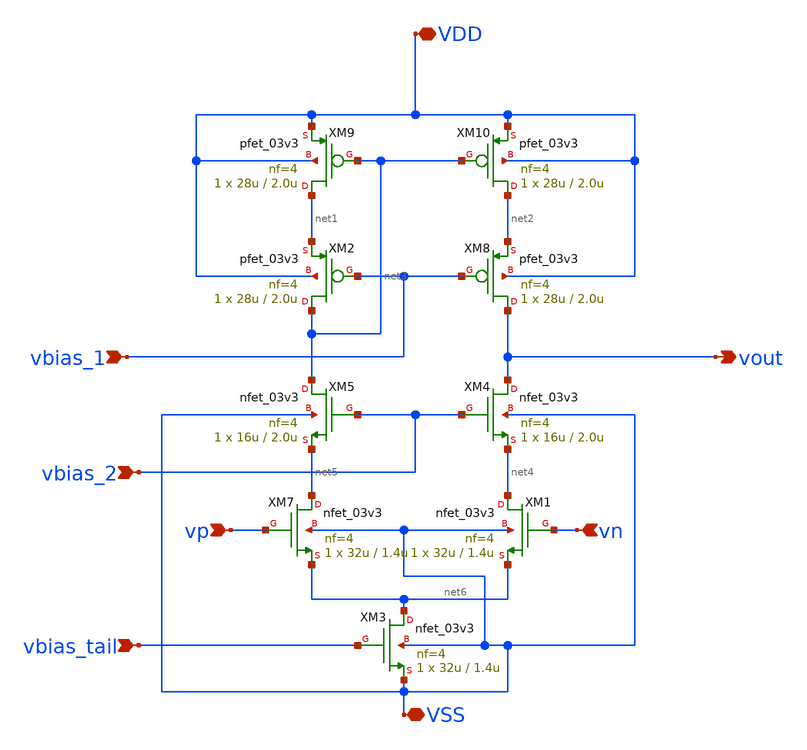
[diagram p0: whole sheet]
** sch_path: xschem/amp_stg_1.sch
**.subckt amp_stg_1 VDD VSS vn vp vout vbias_tail vbias_2 vbias_1
*.iopin VDD
*.iopin VSS
*.ipin vn
*.ipin vp
*.opin vout
*.ipin vbias_tail
*.ipin vbias_2
*.ipin vbias_1
XM2 net3 vbias_1 net1 VDD pfet_03v3 L=2.0u W=28u nf=4 ad='int((nf+1)/2) * W/nf * 0.18u' as='int((nf+2)/2) * W/nf * 0.18u'
+ pd='2*int((nf+1)/2) * (W/nf + 0.18u)' ps='2*int((nf+2)/2) * (W/nf + 0.18u)' nrd='0.18u / W' nrs='0.18u / W'
+ sa=0 sb=0 sd=0 m=1 par=1
XM1 net4 vn net6 VSS nfet_03v3 L=1.4u W=32u nf=4 ad='int((nf+1)/2) * W/nf * 0.18u' as='int((nf+2)/2) * W/nf * 0.18u'
+ pd='2*int((nf+1)/2) * (W/nf + 0.18u)' ps='2*int((nf+2)/2) * (W/nf + 0.18u)' nrd='0.18u / W' nrs='0.18u / W'
+ sa=0 sb=0 sd=0 m=1 par=1
XM3 net6 vbias_tail VSS VSS nfet_03v3 L=1.4u W=32u nf=4 ad='int((nf+1)/2) * W/nf * 0.18u' as='int((nf+2)/2) * W/nf * 0.18u'
+ pd='2*int((nf+1)/2) * (W/nf + 0.18u)' ps='2*int((nf+2)/2) * (W/nf + 0.18u)' nrd='0.18u / W' nrs='0.18u / W'
+ sa=0 sb=0 sd=0 m=1 par=1
XM4 vout vbias_2 net4 VSS nfet_03v3 L=2.0u W=16u nf=4 ad='int((nf+1)/2) * W/nf * 0.18u' as='int((nf+2)/2) * W/nf * 0.18u'
+ pd='2*int((nf+1)/2) * (W/nf + 0.18u)' ps='2*int((nf+2)/2) * (W/nf + 0.18u)' nrd='0.18u / W' nrs='0.18u / W'
+ sa=0 sb=0 sd=0 m=1 par=1
XM5 net3 vbias_2 net5 VSS nfet_03v3 L=2.0u W=16u nf=4 ad='int((nf+1)/2) * W/nf * 0.18u' as='int((nf+2)/2) * W/nf * 0.18u'
+ pd='2*int((nf+1)/2) * (W/nf + 0.18u)' ps='2*int((nf+2)/2) * (W/nf + 0.18u)' nrd='0.18u / W' nrs='0.18u / W'
+ sa=0 sb=0 sd=0 m=1 par=1
XM7 net5 vp net6 VSS nfet_03v3 L=1.4u W=32u nf=4 ad='int((nf+1)/2) * W/nf * 0.18u' as='int((nf+2)/2) * W/nf * 0.18u'
+ pd='2*int((nf+1)/2) * (W/nf + 0.18u)' ps='2*int((nf+2)/2) * (W/nf + 0.18u)' nrd='0.18u / W' nrs='0.18u / W'
+ sa=0 sb=0 sd=0 m=1 par=1
XM8 vout vbias_1 net2 VDD pfet_03v3 L=2.0u W=28u nf=4 ad='int((nf+1)/2) * W/nf * 0.18u' as='int((nf+2)/2) * W/nf * 0.18u'
+ pd='2*int((nf+1)/2) * (W/nf + 0.18u)' ps='2*int((nf+2)/2) * (W/nf + 0.18u)' nrd='0.18u / W' nrs='0.18u / W'
+ sa=0 sb=0 sd=0 m=1 par=1
XM9 net1 net3 VDD VDD pfet_03v3 L=2.0u W=28u nf=4 ad='int((nf+1)/2) * W/nf * 0.18u' as='int((nf+2)/2) * W/nf * 0.18u'
+ pd='2*int((nf+1)/2) * (W/nf + 0.18u)' ps='2*int((nf+2)/2) * (W/nf + 0.18u)' nrd='0.18u / W' nrs='0.18u / W'
+ sa=0 sb=0 sd=0 m=1 par=1
XM10 net2 net3 VDD VDD pfet_03v3 L=2.0u W=28u nf=4 ad='int((nf+1)/2) * W/nf * 0.18u' as='int((nf+2)/2) * W/nf * 0.18u'
+ pd='2*int((nf+1)/2) * (W/nf + 0.18u)' ps='2*int((nf+2)/2) * (W/nf + 0.18u)' nrd='0.18u / W' nrs='0.18u / W'
+ sa=0 sb=0 sd=0 m=1 par=1
**.ends
.end
